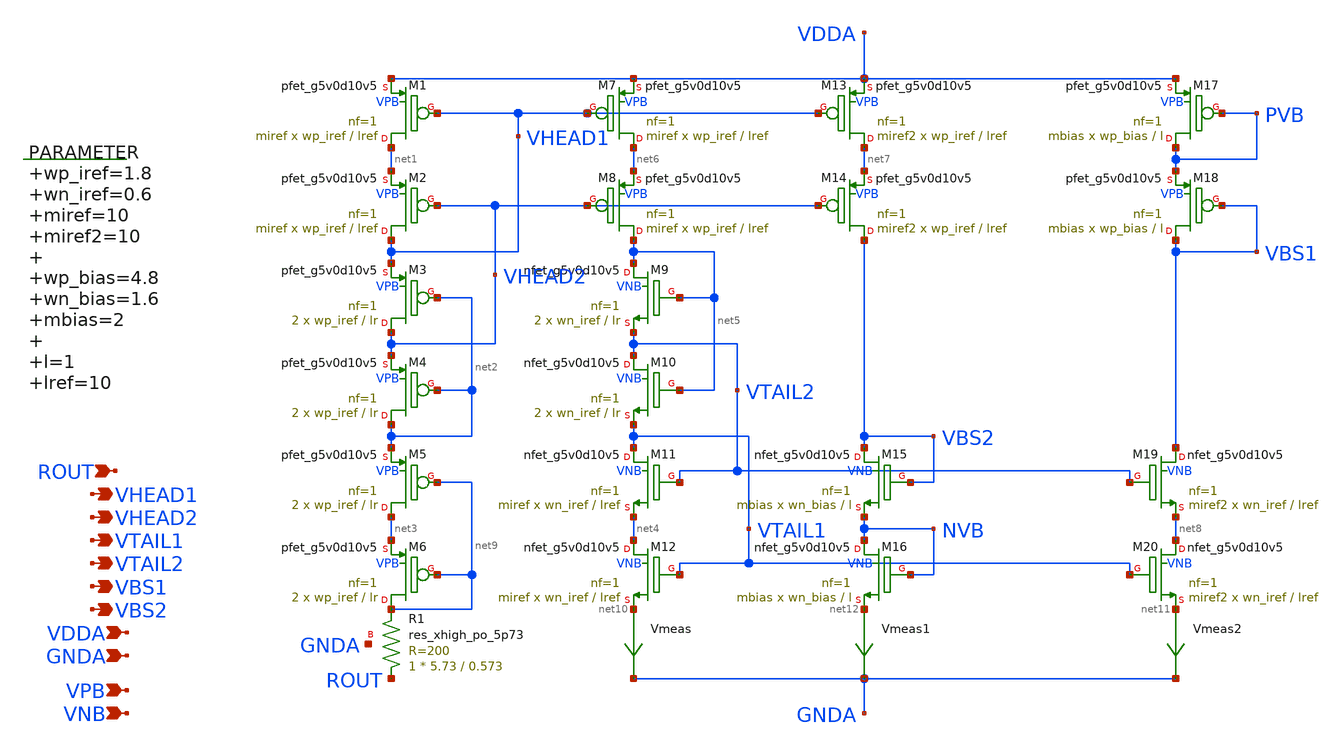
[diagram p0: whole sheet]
** sch_path: xschem/bias_opamp.sch
**.subckt bias_opamp ROUT VHEAD1 VDDA VPB GNDA VNB VHEAD2 VTAIL1 VTAIL2 VBS1 VBS2
*.ipin ROUT
*.opin VHEAD1
*.ipin VDDA
*.ipin VPB
*.ipin GNDA
*.ipin VNB
*.opin VHEAD2
*.opin VTAIL1
*.opin VTAIL2
*.opin VBS1
*.opin VBS2
XM1 net1 VHEAD1 VDDA VPB sky130_fd_pr__pfet_g5v0d10v5 L=lref W=wp_iref nf=1 ad='int((nf+1)/2) * W/nf * 0.29'
+ as='int((nf+2)/2) * W/nf * 0.29' pd='2*int((nf+1)/2) * (W/nf + 0.29)' ps='2*int((nf+2)/2) * (W/nf + 0.29)'
+ nrd='0.29 / W' nrs='0.29 / W' sa=0 sb=0 sd=0 mult=miref m=miref
XM2 VHEAD1 VHEAD2 net1 VPB sky130_fd_pr__pfet_g5v0d10v5 L=lref W=wp_iref nf=1 ad='int((nf+1)/2) * W/nf * 0.29'
+ as='int((nf+2)/2) * W/nf * 0.29' pd='2*int((nf+1)/2) * (W/nf + 0.29)' ps='2*int((nf+2)/2) * (W/nf + 0.29)'
+ nrd='0.29 / W' nrs='0.29 / W' sa=0 sb=0 sd=0 mult=miref m=miref
XM3 VHEAD2 net2 VHEAD1 VPB sky130_fd_pr__pfet_g5v0d10v5 L=lr W=wp_iref nf=1 ad='int((nf+1)/2) * W/nf * 0.29'
+ as='int((nf+2)/2) * W/nf * 0.29' pd='2*int((nf+1)/2) * (W/nf + 0.29)' ps='2*int((nf+2)/2) * (W/nf + 0.29)'
+ nrd='0.29 / W' nrs='0.29 / W' sa=0 sb=0 sd=0 mult=2 m=2
XM7 net6 VHEAD1 VDDA VPB sky130_fd_pr__pfet_g5v0d10v5 L=lref W=wp_iref nf=1 ad='int((nf+1)/2) * W/nf * 0.29'
+ as='int((nf+2)/2) * W/nf * 0.29' pd='2*int((nf+1)/2) * (W/nf + 0.29)' ps='2*int((nf+2)/2) * (W/nf + 0.29)'
+ nrd='0.29 / W' nrs='0.29 / W' sa=0 sb=0 sd=0 mult=miref m=miref
XM8 net5 VHEAD2 net6 VPB sky130_fd_pr__pfet_g5v0d10v5 L=lref W=wp_iref nf=1 ad='int((nf+1)/2) * W/nf * 0.29'
+ as='int((nf+2)/2) * W/nf * 0.29' pd='2*int((nf+1)/2) * (W/nf + 0.29)' ps='2*int((nf+2)/2) * (W/nf + 0.29)'
+ nrd='0.29 / W' nrs='0.29 / W' sa=0 sb=0 sd=0 mult=miref m=miref
XM4 net2 net2 VHEAD2 VPB sky130_fd_pr__pfet_g5v0d10v5 L=lr W=wp_iref nf=1 ad='int((nf+1)/2) * W/nf * 0.29'
+ as='int((nf+2)/2) * W/nf * 0.29' pd='2*int((nf+1)/2) * (W/nf + 0.29)' ps='2*int((nf+2)/2) * (W/nf + 0.29)'
+ nrd='0.29 / W' nrs='0.29 / W' sa=0 sb=0 sd=0 mult=2 m=2
XM5 net3 net9 net2 VPB sky130_fd_pr__pfet_g5v0d10v5 L=lr W=wp_iref nf=1 ad='int((nf+1)/2) * W/nf * 0.29'
+ as='int((nf+2)/2) * W/nf * 0.29' pd='2*int((nf+1)/2) * (W/nf + 0.29)' ps='2*int((nf+2)/2) * (W/nf + 0.29)'
+ nrd='0.29 / W' nrs='0.29 / W' sa=0 sb=0 sd=0 mult=2 m=2
XM6 net9 net9 net3 VPB sky130_fd_pr__pfet_g5v0d10v5 L=lr W=wp_iref nf=1 ad='int((nf+1)/2) * W/nf * 0.29'
+ as='int((nf+2)/2) * W/nf * 0.29' pd='2*int((nf+1)/2) * (W/nf + 0.29)' ps='2*int((nf+2)/2) * (W/nf + 0.29)'
+ nrd='0.29 / W' nrs='0.29 / W' sa=0 sb=0 sd=0 mult=2 m=2
XM9 net5 net5 VTAIL2 VNB sky130_fd_pr__nfet_g5v0d10v5 L=lr W=wn_iref nf=1 ad='int((nf+1)/2) * W/nf * 0.29'
+ as='int((nf+2)/2) * W/nf * 0.29' pd='2*int((nf+1)/2) * (W/nf + 0.29)' ps='2*int((nf+2)/2) * (W/nf + 0.29)'
+ nrd='0.29 / W' nrs='0.29 / W' sa=0 sb=0 sd=0 mult=2 m=2
XM10 VTAIL2 net5 VTAIL1 VNB sky130_fd_pr__nfet_g5v0d10v5 L=lr W=wn_iref nf=1 ad='int((nf+1)/2) * W/nf * 0.29'
+ as='int((nf+2)/2) * W/nf * 0.29' pd='2*int((nf+1)/2) * (W/nf + 0.29)' ps='2*int((nf+2)/2) * (W/nf + 0.29)'
+ nrd='0.29 / W' nrs='0.29 / W' sa=0 sb=0 sd=0 mult=2 m=2
XM11 VTAIL1 VTAIL2 net4 VNB sky130_fd_pr__nfet_g5v0d10v5 L=lref W=wn_iref nf=1 ad='int((nf+1)/2) * W/nf * 0.29'
+ as='int((nf+2)/2) * W/nf * 0.29' pd='2*int((nf+1)/2) * (W/nf + 0.29)' ps='2*int((nf+2)/2) * (W/nf + 0.29)'
+ nrd='0.29 / W' nrs='0.29 / W' sa=0 sb=0 sd=0 mult=miref m=miref
XM12 net4 VTAIL1 net10 VNB sky130_fd_pr__nfet_g5v0d10v5 L=lref W=wn_iref nf=1 ad='int((nf+1)/2) * W/nf * 0.29'
+ as='int((nf+2)/2) * W/nf * 0.29' pd='2*int((nf+1)/2) * (W/nf + 0.29)' ps='2*int((nf+2)/2) * (W/nf + 0.29)'
+ nrd='0.29 / W' nrs='0.29 / W' sa=0 sb=0 sd=0 mult=miref m=miref
.param wp_iref=1.8 wn_iref=0.6 miref=10 miref2=10 wp_bias=4.8 wn_bias=1.6 mbias=2 l=1 lref=10 lr=70
XM13 net7 VHEAD1 VDDA VPB sky130_fd_pr__pfet_g5v0d10v5 L=lref W=wp_iref nf=1 ad='int((nf+1)/2) * W/nf * 0.29'
+ as='int((nf+2)/2) * W/nf * 0.29' pd='2*int((nf+1)/2) * (W/nf + 0.29)' ps='2*int((nf+2)/2) * (W/nf + 0.29)'
+ nrd='0.29 / W' nrs='0.29 / W' sa=0 sb=0 sd=0 mult=miref2 m=miref2
XM14 VBS2 VHEAD2 net7 VPB sky130_fd_pr__pfet_g5v0d10v5 L=lref W=wp_iref nf=1 ad='int((nf+1)/2) * W/nf * 0.29'
+ as='int((nf+2)/2) * W/nf * 0.29' pd='2*int((nf+1)/2) * (W/nf + 0.29)' ps='2*int((nf+2)/2) * (W/nf + 0.29)'
+ nrd='0.29 / W' nrs='0.29 / W' sa=0 sb=0 sd=0 mult=miref2 m=miref2
XM15 VBS2 VBS2 NVB VNB sky130_fd_pr__nfet_g5v0d10v5 L=l W=wn_bias nf=1 ad='int((nf+1)/2) * W/nf * 0.29'
+ as='int((nf+2)/2) * W/nf * 0.29' pd='2*int((nf+1)/2) * (W/nf + 0.29)' ps='2*int((nf+2)/2) * (W/nf + 0.29)'
+ nrd='0.29 / W' nrs='0.29 / W' sa=0 sb=0 sd=0 mult=mbias m=mbias
XM17 PVB PVB VDDA VPB sky130_fd_pr__pfet_g5v0d10v5 L=l W=wp_bias nf=1 ad='int((nf+1)/2) * W/nf * 0.29'
+ as='int((nf+2)/2) * W/nf * 0.29' pd='2*int((nf+1)/2) * (W/nf + 0.29)' ps='2*int((nf+2)/2) * (W/nf + 0.29)'
+ nrd='0.29 / W' nrs='0.29 / W' sa=0 sb=0 sd=0 mult=mbias m=mbias
XM19 VBS1 VTAIL2 net8 VNB sky130_fd_pr__nfet_g5v0d10v5 L=lref W=wn_iref nf=1 ad='int((nf+1)/2) * W/nf * 0.29'
+ as='int((nf+2)/2) * W/nf * 0.29' pd='2*int((nf+1)/2) * (W/nf + 0.29)' ps='2*int((nf+2)/2) * (W/nf + 0.29)'
+ nrd='0.29 / W' nrs='0.29 / W' sa=0 sb=0 sd=0 mult=miref2 m=miref2
XM20 net8 VTAIL1 net11 VNB sky130_fd_pr__nfet_g5v0d10v5 L=lref W=wn_iref nf=1 ad='int((nf+1)/2) * W/nf * 0.29'
+ as='int((nf+2)/2) * W/nf * 0.29' pd='2*int((nf+1)/2) * (W/nf + 0.29)' ps='2*int((nf+2)/2) * (W/nf + 0.29)'
+ nrd='0.29 / W' nrs='0.29 / W' sa=0 sb=0 sd=0 mult=miref2 m=miref2
XR1 ROUT net9 GNDA sky130_fd_pr__res_xhigh_po_5p73 L=0.573 mult=1 m=1
XM18 VBS1 VBS1 PVB VPB sky130_fd_pr__pfet_g5v0d10v5 L=l W=wp_bias nf=1 ad='int((nf+1)/2) * W/nf * 0.29'
+ as='int((nf+2)/2) * W/nf * 0.29' pd='2*int((nf+1)/2) * (W/nf + 0.29)' ps='2*int((nf+2)/2) * (W/nf + 0.29)'
+ nrd='0.29 / W' nrs='0.29 / W' sa=0 sb=0 sd=0 mult=mbias m=mbias
XM16 NVB NVB net12 VNB sky130_fd_pr__nfet_g5v0d10v5 L=l W=wn_bias nf=1 ad='int((nf+1)/2) * W/nf * 0.29'
+ as='int((nf+2)/2) * W/nf * 0.29' pd='2*int((nf+1)/2) * (W/nf + 0.29)' ps='2*int((nf+2)/2) * (W/nf + 0.29)'
+ nrd='0.29 / W' nrs='0.29 / W' sa=0 sb=0 sd=0 mult=mbias m=mbias
Vmeas net10 GNDA 0
.save i(vmeas)
Vmeas1 net12 GNDA 0
.save i(vmeas1)
Vmeas2 net11 GNDA 0
.save i(vmeas2)
**.ends
.end
